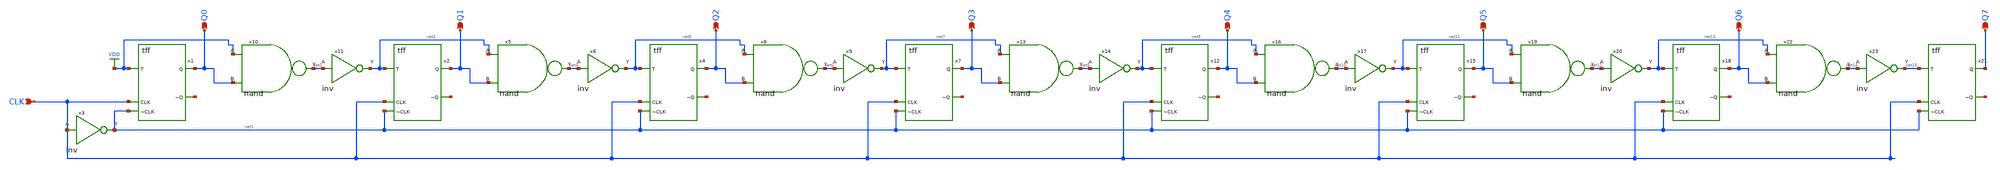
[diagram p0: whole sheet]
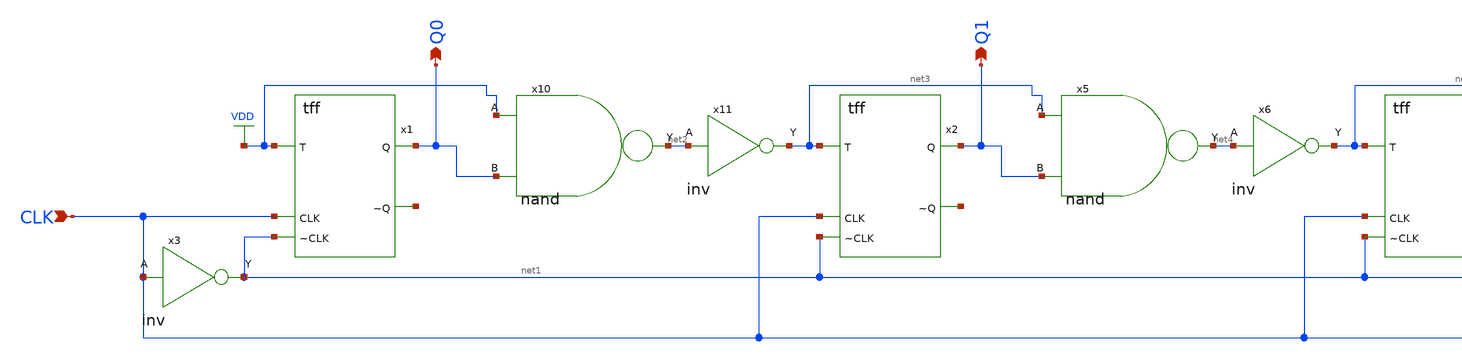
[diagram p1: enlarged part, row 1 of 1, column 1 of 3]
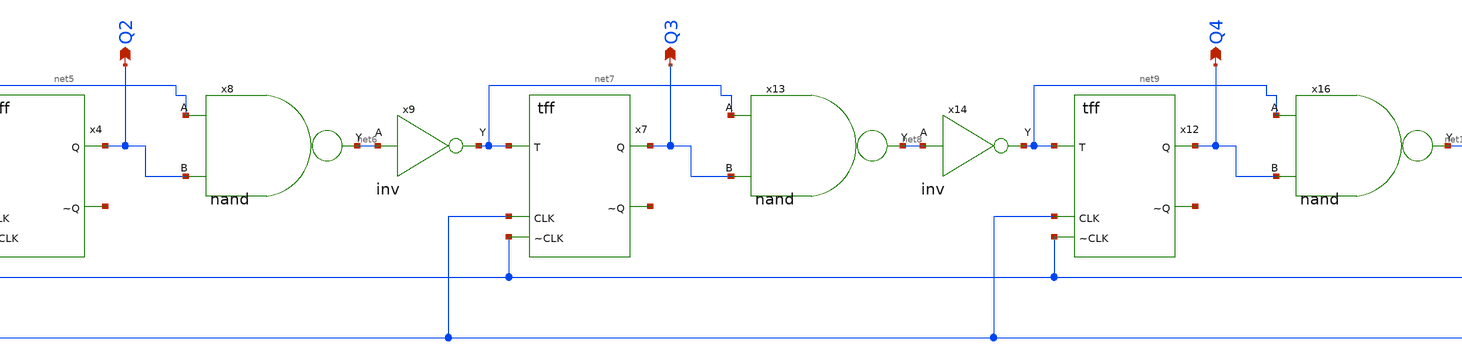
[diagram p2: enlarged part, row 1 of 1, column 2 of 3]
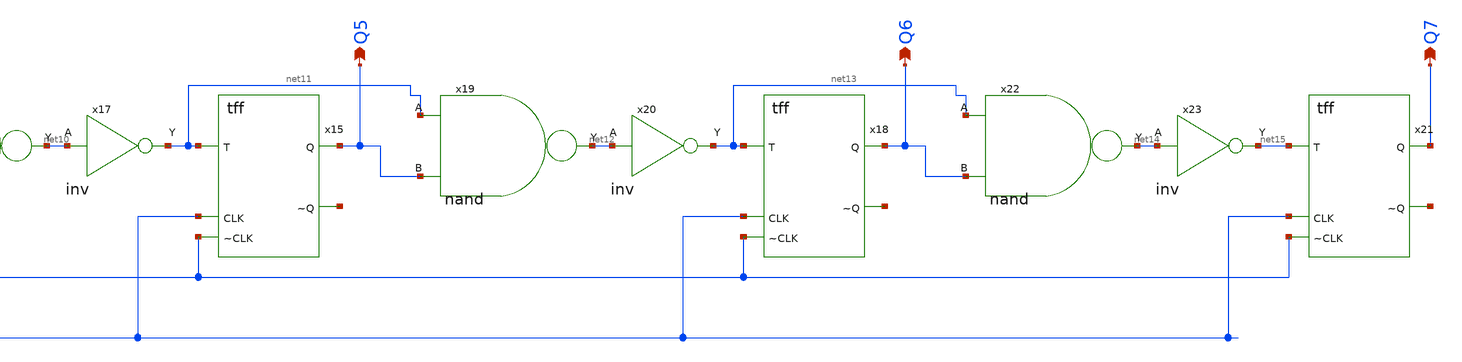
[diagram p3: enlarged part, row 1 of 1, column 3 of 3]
** sch_path: circuits/xschem/counter_8.sch
**.subckt counter_8 CLK Q0 Q1 Q2 Q3 Q4 Q5 Q6 Q7
*.ipin CLK
*.opin Q0
*.opin Q1
*.opin Q2
*.opin Q3
*.opin Q4
*.opin Q5
*.opin Q6
*.opin Q7
x1 VDD Q0 CLK net1 net16 tff
x2 net3 Q1 CLK net1 net17 tff
x3 net1 CLK inv
x10 VDD net2 Q0 nand
x11 net3 net2 inv
x4 net5 Q2 CLK net1 net18 tff
x5 net3 net4 Q1 nand
x6 net5 net4 inv
x7 net7 Q3 CLK net1 net19 tff
x8 net5 net6 Q2 nand
x9 net7 net6 inv
x12 net9 Q4 CLK net1 net20 tff
x13 net7 net8 Q3 nand
x14 net9 net8 inv
x15 net11 Q5 CLK net1 net21 tff
x16 net9 net10 Q4 nand
x17 net11 net10 inv
x18 net13 Q6 CLK net1 net22 tff
x19 net11 net12 Q5 nand
x20 net13 net12 inv
x21 net15 Q7 CLK net1 net23 tff
x22 net13 net14 Q6 nand
x23 net15 net14 inv
**.ends
.GLOBAL VDD
.end
